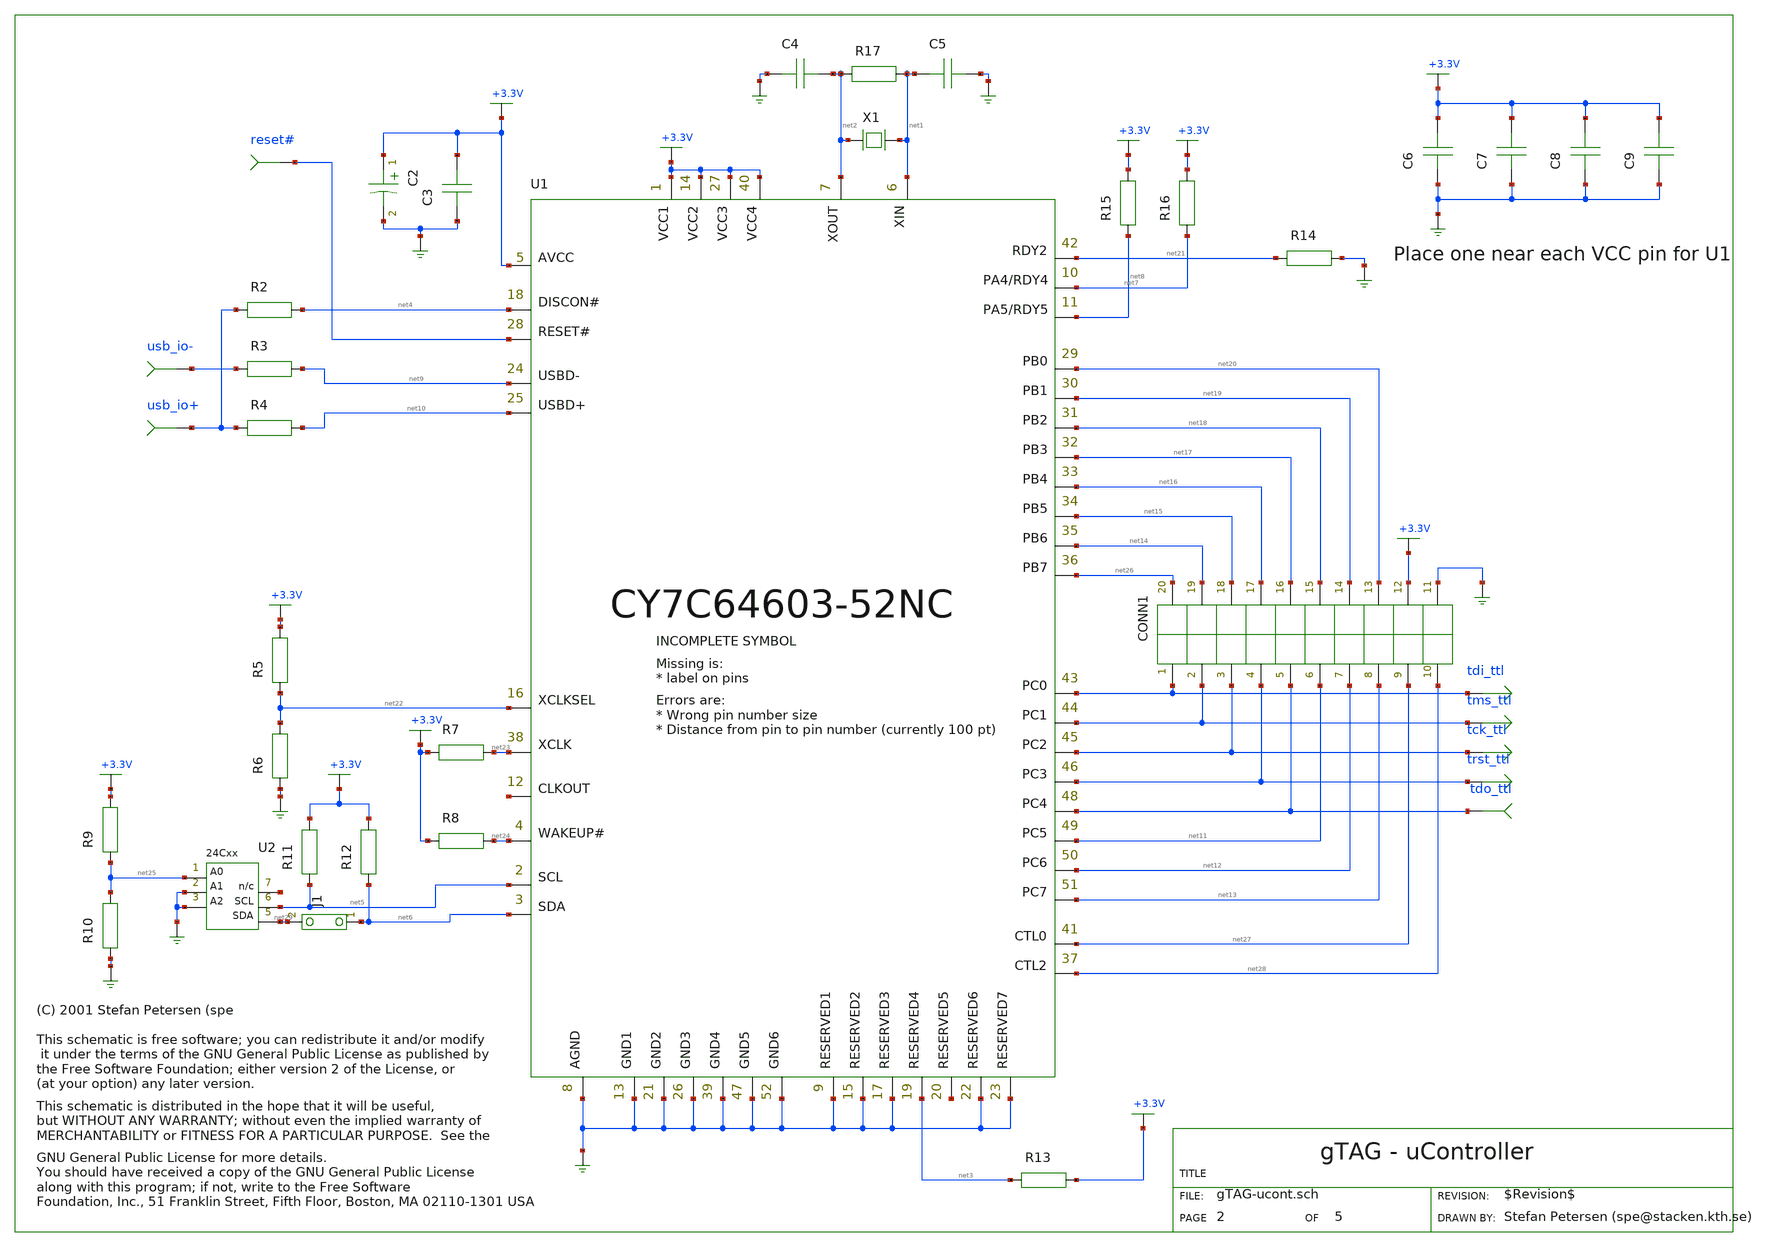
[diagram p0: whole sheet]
** sch_path: xschem-src/xschem_library/gschem_import/gTAG-ucont.sch
* Copyright (C) 1998-2026 Stefan Frederik Schippers
* This program is free software; you can redistribute it and/or modify
* it under the terms of the GNU General Public License as published by
* the Free Software Foundation; either version 2 of the License, or
* (at your option) any later version.
* This program is distributed in the hope that it will be useful,
* but WITHOUT ANY WARRANTY; without even the implied warranty of
* MERCHANTABILITY or FITNESS FOR A PARTICULAR PURPOSE.  See the
* GNU General Public License for more details.
* You should have received a copy of the GNU General Public License
* along with this program; if not, write to the Free Software
* copyleft.sym
**.subckt gTAG-ucont usb_io+ usb_io- tdo_ttl tdi_ttl tms_ttl tck_ttl trst_ttl reset#
U2 net25 GND GND net29 net5 net30 Vcc GND
X1 net2 net1 12MHz
R17 net2 net1 1M
C4 GND net2 30p
C5 net1 GND 30p
R13 net3 +3.3V 10k
R2 usb_io+ net4 1.5k
R12 net6 +3.3V 1k
R11 net5 +3.3V 1k
R6 GND net22 0
R15 net8 +3.3V 10k
R4 usb_io+ net10 22
R3 usb_io- net9 22
R5 net22 +3.3V 0
R7 +3.3V net23 10k
R8 +3.3V net24 10k
C3 GND +3.3V 100n
C2 +3.3V GND 2.2u
U1 +3.3V net5 net6 net24 +3.3V net1 net2 GND GND net7 net8 net31 GND +3.3V GND net22 GND net4 net3
+ net32 GND GND GND net9 net10 GND +3.3V reset# net20 net19 net18 net17 net16 net15 net14 net26 net28 net23
+ GND +3.3V net27 net21 tdi_ttl tms_ttl tck_ttl trst_ttl GND tdo_ttl net11 net12 net13 GND
R16 net7 +3.3V 10k
R14 net21 GND 10k
R10 GND net25 0
R9 net25 +3.3V 0
C6 GND +3.3V 100n
C7 GND +3.3V 100n
C8 GND +3.3V 100n
C9 GND +3.3V 100n
C9
J1 net6 net29
CONN1 tdi_ttl tms_ttl tck_ttl trst_ttl tdo_ttl net11 net12 net13 net27 net28 GND +3.3V net20 net19
+ net18 net17 net16 net15 net14 net26
**.ends
.end
